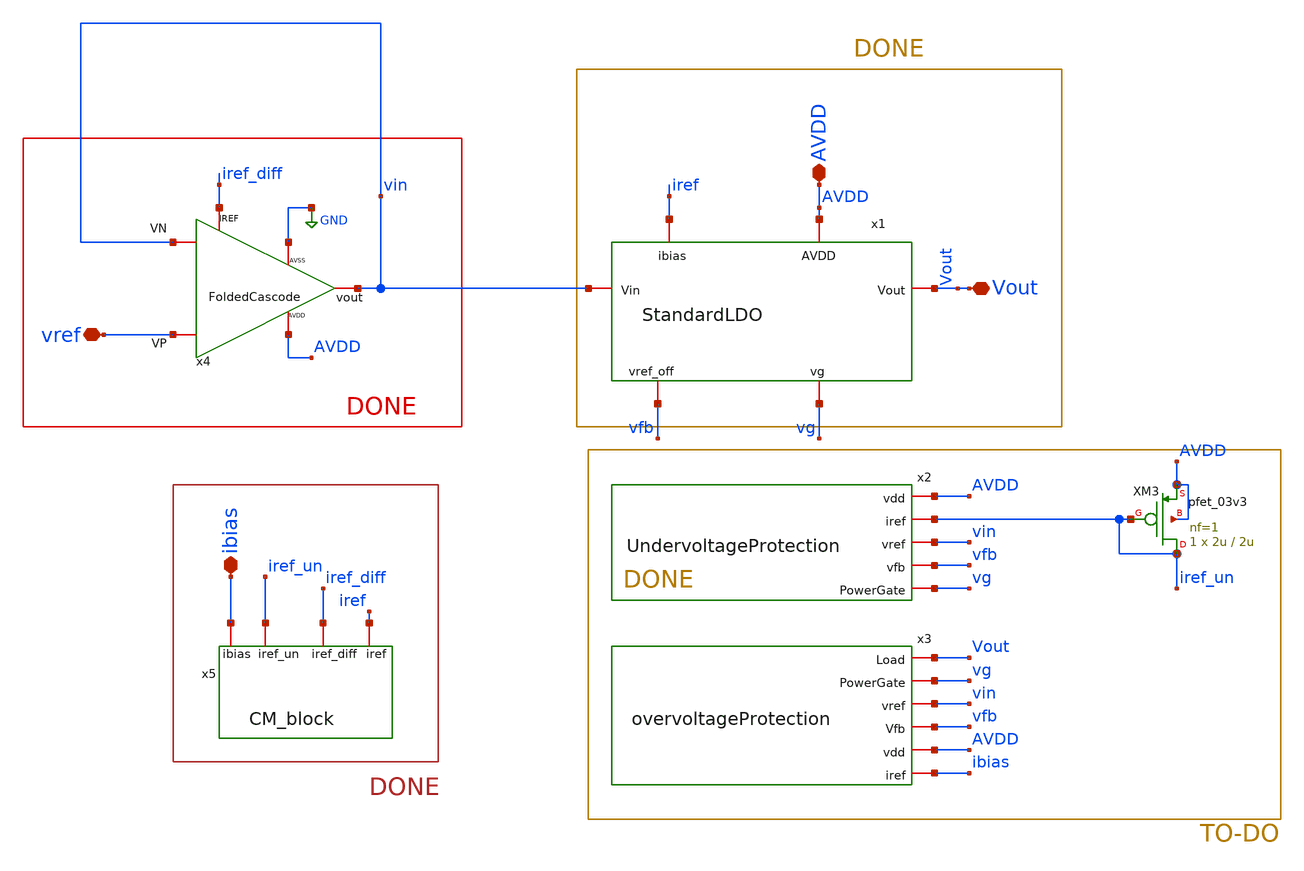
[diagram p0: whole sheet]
** sch_path: Voltage_Reference/LDO/TopLevelLDO.sch
**.subckt TopLevelLDO Vout AVDD ibias vref
*.iopin Vout
*.iopin AVDD
*.iopin ibias
*.iopin vref
x1 iref AVDD vg vin Vout vfb StandardLDO
x2 AVDD iref_un vin vfb vg UndervoltageProtection
x3 Vout vg vin vfb AVDD ibias overvoltageProtection
XM3 iref_un iref_un AVDD AVDD pfet_03v3 L=2u W=2u nf=1 ad='int((nf+1)/2) * W/nf * 0.18u' as='int((nf+2)/2) * W/nf * 0.18u'
+ pd='2*int((nf+1)/2) * (W/nf + 0.18u)' ps='2*int((nf+2)/2) * (W/nf + 0.18u)' nrd='0.18u / W' nrs='0.18u / W'
+ sa=0 sb=0 sd=0 m=1
x4 vref vin vin iref_diff AVDD GND FoldedCascode
x5 ibias iref_un iref_diff iref CM_block
**.ends
.GLOBAL GND
.end
